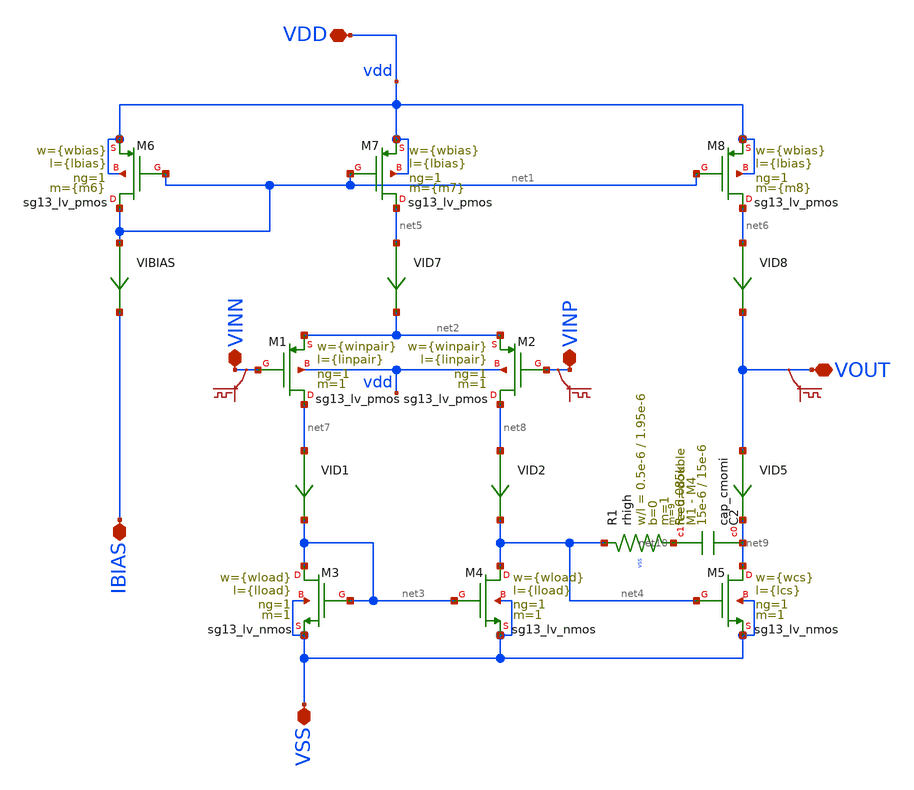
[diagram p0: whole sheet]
** sch_path: xschem/ota_cmos5l/ota_cmos5l.sch
**.subckt ota_cmos5l IBIAS VDD VSS VOUT VINP VINN
*.iopin IBIAS
*.iopin VDD
*.iopin VSS
*.iopin VOUT
*.iopin VINP
*.iopin VINN
XM6 net1 net1 vdd vdd sg13_lv_pmos w={wbias} l={lbias} ng=1 m={m6} mm_ok=1
XM7 net5 net1 vdd vdd sg13_lv_pmos w={wbias} l={lbias} ng=1 m={m7} mm_ok=1
XM8 net6 net1 vdd vdd sg13_lv_pmos w={wbias} l={lbias} ng=1 m={m8} mm_ok=1
XM1 net7 VINN net2 vdd sg13_lv_pmos w={winpair} l={linpair} ng=1 m=1 mm_ok=1
XM2 net8 VINP net2 vdd sg13_lv_pmos w={winpair} l={linpair} ng=1 m=1 mm_ok=1
XM3 net3 net3 VSS VSS sg13_lv_nmos w={wload} l={lload} ng=1 m=1 mm_ok=1
XM4 net4 net3 VSS VSS sg13_lv_nmos w={wload} l={lload} ng=1 m=1 mm_ok=1
XM5 net9 net4 VSS VSS sg13_lv_nmos w={wcs} l={lcs} ng=1 m=1 mm_ok=1
XR1 net4 net10 vss rhigh w=0.5e-6 l=1.95e-6 m=1 b=0 mm_ok=1
VIBIAS net1 IBIAS 0
.save i(vibias)
VID7 net5 net2 0
.save i(vid7)
VID8 net6 VOUT 0
.save i(vid8)
.save v(vinp)
.save v(vinn)
.save v(vout)
VID1 net7 net3 0
.save i(vid1)
VID2 net8 net4 0
.save i(vid2)
VID5 VOUT net9 0
.save i(vid5)
XC2 net9 net10 cap_cmomi w=15e-6 l=15e-6 mmin=1 mmax=4 feed=double subblock=0 m=9 mm_ok=1
**.ends
.end
